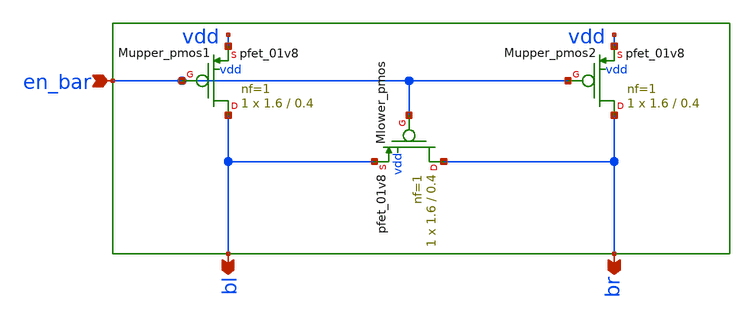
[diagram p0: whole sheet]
** sch_path: sram_2_64_scn4m_lcc/precharge_0.sch
**.subckt precharge_0 bl br en_bar
*.opin bl
*.opin br
*.ipin en_bar
XMupper_pmos1 bl en_bar vdd vdd sky130_fd_pr__pfet_01v8 L=0.4 W=1.6 nf=1 ad='int((nf+1)/2) * W/nf * 0.29'
+ as='int((nf+2)/2) * W/nf * 0.29' pd='2*int((nf+1)/2) * (W/nf + 0.29)' ps='2*int((nf+2)/2) * (W/nf + 0.29)'
+ nrd='0.29 / W' nrs='0.29 / W' sa=0 sb=0 sd=0 mult=1 m=1
XMupper_pmos2 br en_bar vdd vdd sky130_fd_pr__pfet_01v8 L=0.4 W=1.6 nf=1 ad='int((nf+1)/2) * W/nf * 0.29'
+ as='int((nf+2)/2) * W/nf * 0.29' pd='2*int((nf+1)/2) * (W/nf + 0.29)' ps='2*int((nf+2)/2) * (W/nf + 0.29)'
+ nrd='0.29 / W' nrs='0.29 / W' sa=0 sb=0 sd=0 mult=1 m=1
XMlower_pmos br en_bar bl vdd sky130_fd_pr__pfet_01v8 L=0.4 W=1.6 nf=1 ad='int((nf+1)/2) * W/nf * 0.29'
+ as='int((nf+2)/2) * W/nf * 0.29' pd='2*int((nf+1)/2) * (W/nf + 0.29)' ps='2*int((nf+2)/2) * (W/nf + 0.29)'
+ nrd='0.29 / W' nrs='0.29 / W' sa=0 sb=0 sd=0 mult=1 m=1
**.ends
.end
